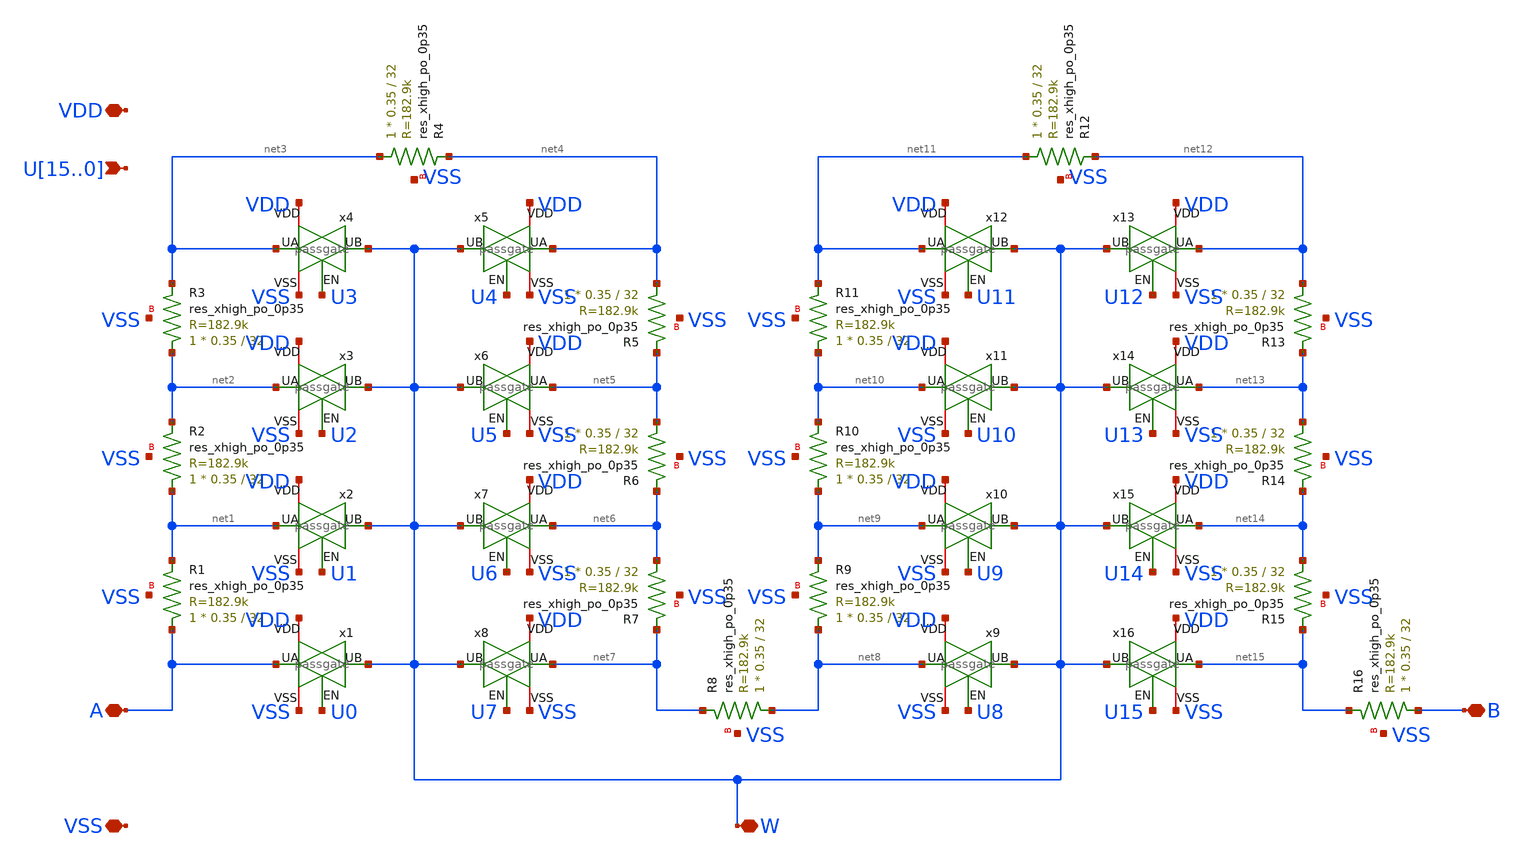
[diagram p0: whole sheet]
** sch_path: xschem/digipot_1hot.sch
**.subckt digipot_1hot VDD VSS A B W U15,U14,U13,U12,U11,U10,U9,U8,U7,U6,U5,U4,U3,U2,U1,U0
*.iopin VDD
*.iopin VSS
*.iopin A
*.iopin B
*.iopin W
*.ipin U15,U14,U13,U12,U11,U10,U9,U8,U7,U6,U5,U4,U3,U2,U1,U0
XR1 A net1 VSS sky130_fd_pr__res_xhigh_po_0p35 L=32 mult=1 m=1
XR2 net1 net2 VSS sky130_fd_pr__res_xhigh_po_0p35 L=32 mult=1 m=1
XR3 net2 net3 VSS sky130_fd_pr__res_xhigh_po_0p35 L=32 mult=1 m=1
XR4 net3 net4 VSS sky130_fd_pr__res_xhigh_po_0p35 L=32 mult=1 m=1
XR5 net4 net5 VSS sky130_fd_pr__res_xhigh_po_0p35 L=32 mult=1 m=1
x1 VDD A W U0 VSS passgate
x2 VDD net1 W U1 VSS passgate
x3 VDD net2 W U2 VSS passgate
x4 VDD net3 W U3 VSS passgate
x5 VDD net4 W U4 VSS passgate
XR6 net5 net6 VSS sky130_fd_pr__res_xhigh_po_0p35 L=32 mult=1 m=1
x6 VDD net5 W U5 VSS passgate
XR7 net6 net7 VSS sky130_fd_pr__res_xhigh_po_0p35 L=32 mult=1 m=1
x7 VDD net6 W U6 VSS passgate
XR8 net8 net7 VSS sky130_fd_pr__res_xhigh_po_0p35 L=32 mult=1 m=1
x8 VDD net7 W U7 VSS passgate
XR9 net8 net9 VSS sky130_fd_pr__res_xhigh_po_0p35 L=32 mult=1 m=1
XR10 net9 net10 VSS sky130_fd_pr__res_xhigh_po_0p35 L=32 mult=1 m=1
XR11 net10 net11 VSS sky130_fd_pr__res_xhigh_po_0p35 L=32 mult=1 m=1
XR12 net11 net12 VSS sky130_fd_pr__res_xhigh_po_0p35 L=32 mult=1 m=1
XR13 net12 net13 VSS sky130_fd_pr__res_xhigh_po_0p35 L=32 mult=1 m=1
x9 VDD net8 W U8 VSS passgate
x10 VDD net9 W U9 VSS passgate
x11 VDD net10 W U10 VSS passgate
x12 VDD net11 W U11 VSS passgate
x13 VDD net12 W U12 VSS passgate
XR14 net13 net14 VSS sky130_fd_pr__res_xhigh_po_0p35 L=32 mult=1 m=1
x14 VDD net13 W U13 VSS passgate
XR15 net14 net15 VSS sky130_fd_pr__res_xhigh_po_0p35 L=32 mult=1 m=1
x15 VDD net14 W U14 VSS passgate
x16 VDD net15 W U15 VSS passgate
XR16 B net15 VSS sky130_fd_pr__res_xhigh_po_0p35 L=32 mult=1 m=1
**.ends

* expanding   symbol:  passgate.sym # of pins=5
** sym_path: xschem/passgate.sym
** sch_path: xschem/passgate.sch
.subckt passgate VDD UA UB EN VSS
*.iopin VSS
*.iopin VDD
*.iopin UA
*.iopin UB
*.ipin EN
XM1 UA EN UB VSS sky130_fd_pr__nfet_g5v0d10v5 L=0.5 W=0.65 nf=1 ad='int((1 + 1)/2) * 0.65 / 1 * 0.29'
+ as='int((1 + 2)/2) * 0.65 / 1 * 0.29' pd='2*int((1 + 1)/2) * (0.65 / 1 + 0.29)' ps='2*int((1 + 2)/2) * (0.65 / 1 + 0.29)'
+ nrd='0.29 / 0.65 ' nrs='0.29 / 0.65 ' sa=0 sb=0 sd=0 mult=1 m=1
XM2 UA net1 UB VDD sky130_fd_pr__pfet_g5v0d10v5 L=0.5 W=1 nf=1 ad='int((1 + 1)/2) * 1 / 1 * 0.29' as='int((1 + 2)/2) * 1 / 1 * 0.29'
+ pd='2*int((1 + 1)/2) * (1 / 1 + 0.29)' ps='2*int((1 + 2)/2) * (1 / 1 + 0.29)' nrd='0.29 / 1 ' nrs='0.29 / 1 '
+ sa=0 sb=0 sd=0 mult=1 m=1
x1 VDD EN net1 VSS inverter
.ends


* expanding   symbol:  inverter.sym # of pins=4
** sym_path: xschem/inverter.sym
** sch_path: xschem/inverter.sch
.subckt inverter VDD IN OUT VSS
*.iopin VSS
*.iopin VDD
*.ipin IN
*.opin OUT
XM1 OUT IN VSS VSS sky130_fd_pr__nfet_g5v0d10v5 L=0.5 W=0.65 nf=1 ad='int((1 + 1)/2) * 0.65 / 1 * 0.29'
+ as='int((1 + 2)/2) * 0.65 / 1 * 0.29' pd='2*int((1 + 1)/2) * (0.65 / 1 + 0.29)' ps='2*int((1 + 2)/2) * (0.65 / 1 + 0.29)'
+ nrd='0.29 / 0.65 ' nrs='0.29 / 0.65 ' sa=0 sb=0 sd=0 mult=1 m=1
XM2 OUT IN VDD VDD sky130_fd_pr__pfet_g5v0d10v5 L=0.5 W=1 nf=1 ad='int((1 + 1)/2) * 1 / 1 * 0.29' as='int((1 + 2)/2) * 1 / 1 * 0.29'
+ pd='2*int((1 + 1)/2) * (1 / 1 + 0.29)' ps='2*int((1 + 2)/2) * (1 / 1 + 0.29)' nrd='0.29 / 1 ' nrs='0.29 / 1 '
+ sa=0 sb=0 sd=0 mult=1 m=1
.ends

.end
